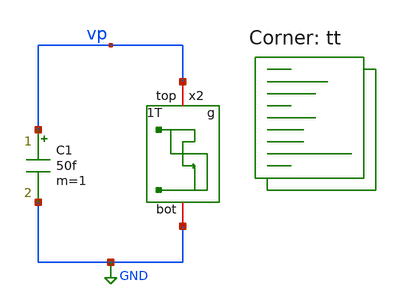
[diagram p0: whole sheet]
** sch_path: xschem/tb/dschr_nwk_type_g_tb.sch
**.subckt dschr_nwk_type_g_tb
C1 vp GND 50f m=1
x2 vp GND dschr_nwk_type_g L=0.15 W=0.5
**** begin user architecture code
.lib $::SKYWATER_MODELS/sky130.lib.spice tt


.include $::netlist_dir/ctrl_sims.spice


**** end user architecture code
**.ends

* expanding   symbol:  dschr_nwks/dschr_nwk_type_g.sym # of pins=2
** sym_path: xschem/dschr_nwks/dschr_nwk_type_g.sym
** sch_path: xschem/dschr_nwks/dschr_nwk_type_g.sch
.subckt dschr_nwk_type_g top bot  L=0.18 W=1
*.iopin top
*.iopin bot
XM1 top top bot bot sky130_fd_pr__nfet_01v8 L='L' W='W' nf=1 ad='int((nf+1)/2) * W/nf * 0.29' as='int((nf+2)/2) * W/nf * 0.29'
+ pd='2*int((nf+1)/2) * (W/nf + 0.29)' ps='2*int((nf+2)/2) * (W/nf + 0.29)' nrd='0.29 / W' nrs='0.29 / W'
+ sa=0 sb=0 sd=0 mult=1 m=1
.ends

.GLOBAL GND
.end
